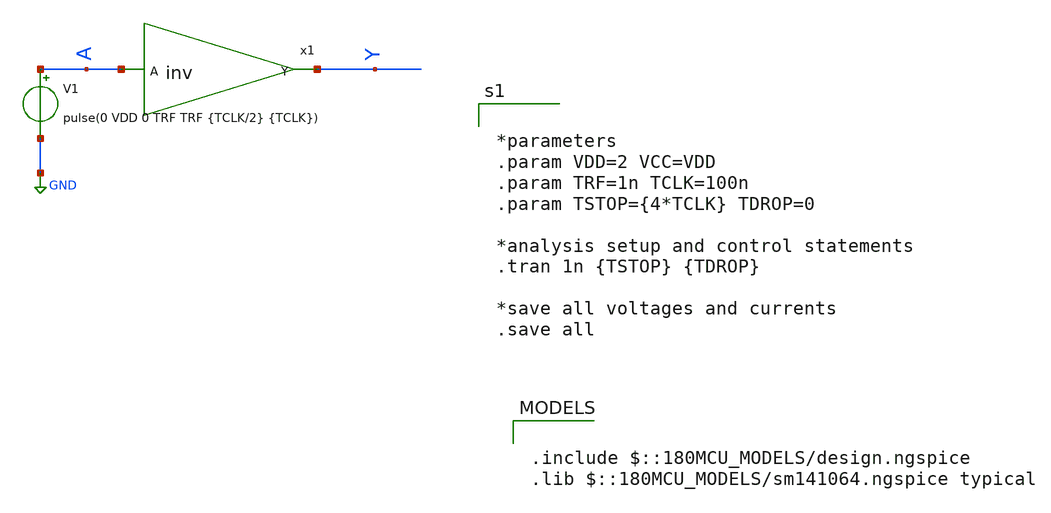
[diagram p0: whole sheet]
** sch_path: XSCHEM Files/inv_tb.sch
**.subckt inv_tb
V1 A GND pulse(0 VDD 0 TRF TRF {TCLK/2} {TCLK})
x1 Y A inv
**** begin user architecture code


*parameters
.param VDD=2 VCC=VDD
.param TRF=1n TCLK=100n
.param TSTOP={4*TCLK} TDROP=0

*analysis setup and control statements
.tran 1n {TSTOP} {TDROP}

*save all voltages and currents
.save all



.include $::180MCU_MODELS/design.ngspice
.lib $::180MCU_MODELS/sm141064.ngspice typical

**** end user architecture code
**.ends

* expanding   symbol:  /home/tare/Desktop/Final/inv.sym # of pins=2
** sym_path: XSCHEM Files/inv.sym
** sch_path: XSCHEM Files/inv.sch
.subckt inv Y A
*.ipin A
*.opin Y
**** begin user architecture code


*inverter model
a1 A Yi my_inv
.model my_inv d_inverter(rise_delay = 1e-9 fall_delay = 1e-9                         input_load =
+ 1e-12)

*force netlisting of digital outputs
v1 Yi Y 0


**** end user architecture code
.ends

.GLOBAL GND
.end
